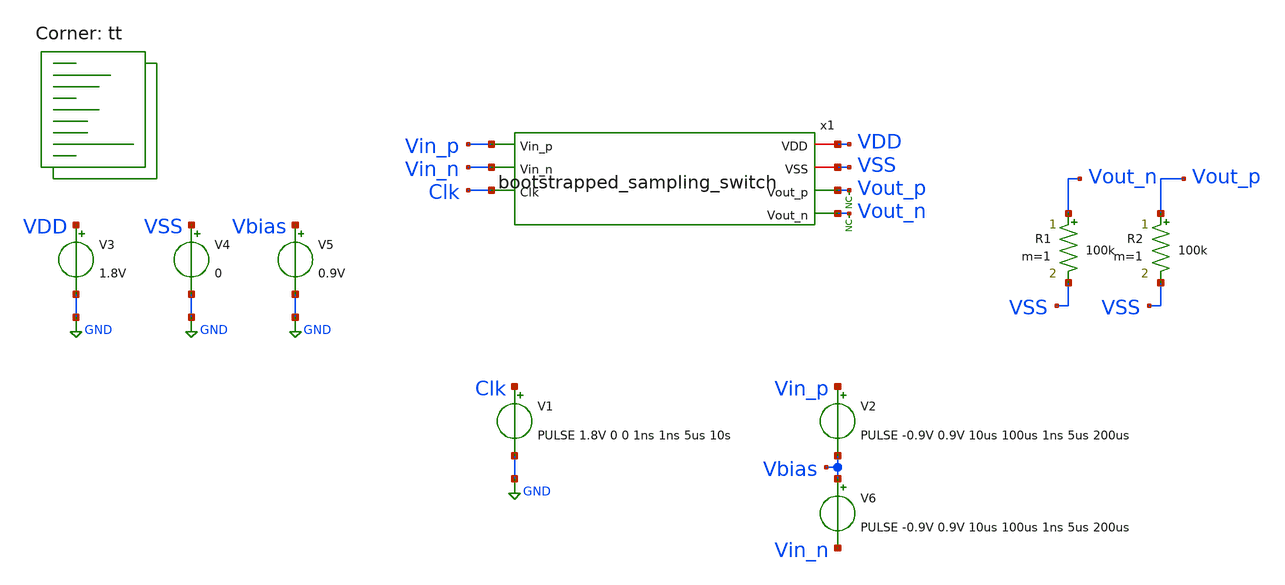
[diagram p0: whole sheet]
** sch_path: xschem/tests/bootstrapped_sampling_switch/bootstrapped_sampling_switch_load_test.sch
**.subckt bootstrapped_sampling_switch_load_test
V3 VDD GND 1.8V
V4 VSS GND 0
x1 VDD Vin_p VSS Vin_n Clk Vout_p Vout_n bootstrapped_sampling_switch
V1 Clk GND PULSE 1.8V 0 0 1ns 1ns 5us 10s
V2 Vin_p Vbias PULSE -0.9V 0.9V 10us 100us 1ns 5us 200us
* noconn Vout_p
* noconn Vout_n
V5 Vbias GND 0.9V
V6 Vbias Vin_n PULSE -0.9V 0.9V 10us 100us 1ns 5us 200us
R1 Vout_n VSS 100k m=1
R2 Vout_p VSS 100k m=1
**** begin user architecture code
 *.lib $::SKYWATER_MODELS/sky130.lib.spice tt
.include $::SKYWATER_STDCELLS/sky130_fd_sc_hd.spice


.options acct list
.temp 25
*vvcc VDD 0 dc 1.8
*vvss VSS 0 0
.control
save all
tran 0.1u 110u
*plot RST_PLS clk+2 Pulse+4
plot Vin_p-Vin_n Vout_p-Vout_n clk-4
plot Vout_p-Vout_n clk-4
plot Vout_p Vout_n clk-4
plot x1.net4-x1.net3
plot x1.net9-x1.net8
write bootstrapped_sampling_switch_load_test.raw
.endc


.lib $::SKYWATER_MODELS/sky130.lib.spice tt
**** end user architecture code
**.ends

* expanding   symbol:  src/bootstrapped_sampling_switch/bootstrapped_sampling_switch.sym # of pins=7
** sym_path: xschem/src/bootstrapped_sampling_switch/bootstrapped_sampling_switch.sym
** sch_path: xschem/src/bootstrapped_sampling_switch/bootstrapped_sampling_switch.sch
.subckt bootstrapped_sampling_switch VDD Vin_p VSS Vin_n Clk Vout_p Vout_n
*.iopin VDD
*.ipin Vin_p
*.opin Vout_p
*.iopin VSS
*.opin Vout_n
*.ipin Vin_n
*.ipin Clk
XM1 net3 Clk_n VSS VSS sky130_fd_pr__nfet_01v8 L=0.15 W=0.91 nf=1 ad='int((nf+1)/2) * W/nf * 0.29' as='int((nf+2)/2) * W/nf * 0.29'
+ pd='2*int((nf+1)/2) * (W/nf + 0.29)' ps='2*int((nf+2)/2) * (W/nf + 0.29)' nrd='0.29 / W' nrs='0.29 / W'
+ sa=0 sb=0 sd=0 mult=8 m=8
XM2 net1 Clk VDD VDD sky130_fd_pr__pfet_01v8 L=0.15 W=1.605 nf=1 ad='int((nf+1)/2) * W/nf * 0.29' as='int((nf+2)/2) * W/nf * 0.29'
+ pd='2*int((nf+1)/2) * (W/nf + 0.29)' ps='2*int((nf+2)/2) * (W/nf + 0.29)' nrd='0.29 / W' nrs='0.29 / W'
+ sa=0 sb=0 sd=0 mult=1 m=1
XM3 net1 Clk net3 VSS sky130_fd_pr__nfet_01v8 L=0.15 W=0.91 nf=1 ad='int((nf+1)/2) * W/nf * 0.29' as='int((nf+2)/2) * W/nf * 0.29'
+ pd='2*int((nf+1)/2) * (W/nf + 0.29)' ps='2*int((nf+2)/2) * (W/nf + 0.29)' nrd='0.29 / W' nrs='0.29 / W'
+ sa=0 sb=0 sd=0 mult=1 m=1
XC1 net2 net3 sky130_fd_pr__cap_mim_m3_1 W=30 L=30 MF=1 m=1
XM4 net2 net4 VDD net2 sky130_fd_pr__pfet_01v8 L=0.15 W=5 nf=1 ad='int((nf+1)/2) * W/nf * 0.29' as='int((nf+2)/2) * W/nf * 0.29'
+ pd='2*int((nf+1)/2) * (W/nf + 0.29)' ps='2*int((nf+2)/2) * (W/nf + 0.29)' nrd='0.29 / W' nrs='0.29 / W'
+ sa=0 sb=0 sd=0 mult=1 m=1
XM5 net4 net1 net2 net2 sky130_fd_pr__pfet_01v8 L=0.15 W=1.605 nf=1 ad='int((nf+1)/2) * W/nf * 0.29'
+ as='int((nf+2)/2) * W/nf * 0.29' pd='2*int((nf+1)/2) * (W/nf + 0.29)' ps='2*int((nf+2)/2) * (W/nf + 0.29)'
+ nrd='0.29 / W' nrs='0.29 / W' sa=0 sb=0 sd=0 mult=1 m=1
XM6 net1 net4 net3 VSS sky130_fd_pr__nfet_01v8 L=0.15 W=0.91 nf=1 ad='int((nf+1)/2) * W/nf * 0.29' as='int((nf+2)/2) * W/nf * 0.29'
+ pd='2*int((nf+1)/2) * (W/nf + 0.29)' ps='2*int((nf+2)/2) * (W/nf + 0.29)' nrd='0.29 / W' nrs='0.29 / W'
+ sa=0 sb=0 sd=0 mult=1 m=1
XM7 Vin_p net4 net3 VSS sky130_fd_pr__nfet_01v8 L=0.15 W=0.91 nf=1 ad='int((nf+1)/2) * W/nf * 0.29' as='int((nf+2)/2) * W/nf * 0.29'
+ pd='2*int((nf+1)/2) * (W/nf + 0.29)' ps='2*int((nf+2)/2) * (W/nf + 0.29)' nrd='0.29 / W' nrs='0.29 / W'
+ sa=0 sb=0 sd=0 mult=1 m=1
XM8 Vin_p net4 Vout_p VSS sky130_fd_pr__nfet_01v8 L=0.15 W=0.91 nf=1 ad='int((nf+1)/2) * W/nf * 0.29'
+ as='int((nf+2)/2) * W/nf * 0.29' pd='2*int((nf+1)/2) * (W/nf + 0.29)' ps='2*int((nf+2)/2) * (W/nf + 0.29)'
+ nrd='0.29 / W' nrs='0.29 / W' sa=0 sb=0 sd=0 mult=75 m=75
XM9 net4 VDD net5 VSS sky130_fd_pr__nfet_01v8 L=0.15 W=0.91 nf=1 ad='int((nf+1)/2) * W/nf * 0.29' as='int((nf+2)/2) * W/nf * 0.29'
+ pd='2*int((nf+1)/2) * (W/nf + 0.29)' ps='2*int((nf+2)/2) * (W/nf + 0.29)' nrd='0.29 / W' nrs='0.29 / W'
+ sa=0 sb=0 sd=0 mult=2 m=2
XM10 net5 Clk_n VSS VSS sky130_fd_pr__nfet_01v8 L=0.15 W=0.91 nf=1 ad='int((nf+1)/2) * W/nf * 0.29' as='int((nf+2)/2) * W/nf * 0.29'
+ pd='2*int((nf+1)/2) * (W/nf + 0.29)' ps='2*int((nf+2)/2) * (W/nf + 0.29)' nrd='0.29 / W' nrs='0.29 / W'
+ sa=0 sb=0 sd=0 mult=1 m=1
x1 Clk VSS VSS VDD VDD Clk_n sky130_fd_sc_hd__clkinv_1
XM11 net8 Clk_n VSS VSS sky130_fd_pr__nfet_01v8 L=0.15 W=0.91 nf=1 ad='int((nf+1)/2) * W/nf * 0.29' as='int((nf+2)/2) * W/nf * 0.29'
+ pd='2*int((nf+1)/2) * (W/nf + 0.29)' ps='2*int((nf+2)/2) * (W/nf + 0.29)' nrd='0.29 / W' nrs='0.29 / W'
+ sa=0 sb=0 sd=0 mult=8 m=8
XM12 net6 Clk VDD VDD sky130_fd_pr__pfet_01v8 L=0.15 W=1.605 nf=1 ad='int((nf+1)/2) * W/nf * 0.29' as='int((nf+2)/2) * W/nf * 0.29'
+ pd='2*int((nf+1)/2) * (W/nf + 0.29)' ps='2*int((nf+2)/2) * (W/nf + 0.29)' nrd='0.29 / W' nrs='0.29 / W'
+ sa=0 sb=0 sd=0 mult=1 m=1
XM13 net6 Clk net8 VSS sky130_fd_pr__nfet_01v8 L=0.15 W=0.91 nf=1 ad='int((nf+1)/2) * W/nf * 0.29' as='int((nf+2)/2) * W/nf * 0.29'
+ pd='2*int((nf+1)/2) * (W/nf + 0.29)' ps='2*int((nf+2)/2) * (W/nf + 0.29)' nrd='0.29 / W' nrs='0.29 / W'
+ sa=0 sb=0 sd=0 mult=1 m=1
XC2 net7 net8 sky130_fd_pr__cap_mim_m3_1 W=30 L=30 MF=1 m=1
XM14 net7 net9 VDD net7 sky130_fd_pr__pfet_01v8 L=0.15 W=5 nf=1 ad='int((nf+1)/2) * W/nf * 0.29' as='int((nf+2)/2) * W/nf * 0.29'
+ pd='2*int((nf+1)/2) * (W/nf + 0.29)' ps='2*int((nf+2)/2) * (W/nf + 0.29)' nrd='0.29 / W' nrs='0.29 / W'
+ sa=0 sb=0 sd=0 mult=1 m=1
XM15 net9 net6 net7 net7 sky130_fd_pr__pfet_01v8 L=0.15 W=1.605 nf=1 ad='int((nf+1)/2) * W/nf * 0.29'
+ as='int((nf+2)/2) * W/nf * 0.29' pd='2*int((nf+1)/2) * (W/nf + 0.29)' ps='2*int((nf+2)/2) * (W/nf + 0.29)'
+ nrd='0.29 / W' nrs='0.29 / W' sa=0 sb=0 sd=0 mult=1 m=1
XM16 net6 net9 net8 VSS sky130_fd_pr__nfet_01v8 L=0.15 W=0.91 nf=1 ad='int((nf+1)/2) * W/nf * 0.29' as='int((nf+2)/2) * W/nf * 0.29'
+ pd='2*int((nf+1)/2) * (W/nf + 0.29)' ps='2*int((nf+2)/2) * (W/nf + 0.29)' nrd='0.29 / W' nrs='0.29 / W'
+ sa=0 sb=0 sd=0 mult=1 m=1
XM17 Vin_n net9 net8 VSS sky130_fd_pr__nfet_01v8 L=0.15 W=0.91 nf=1 ad='int((nf+1)/2) * W/nf * 0.29'
+ as='int((nf+2)/2) * W/nf * 0.29' pd='2*int((nf+1)/2) * (W/nf + 0.29)' ps='2*int((nf+2)/2) * (W/nf + 0.29)'
+ nrd='0.29 / W' nrs='0.29 / W' sa=0 sb=0 sd=0 mult=1 m=1
XM18 Vin_n net9 Vout_n VSS sky130_fd_pr__nfet_01v8 L=0.15 W=0.91 nf=1 ad='int((nf+1)/2) * W/nf * 0.29'
+ as='int((nf+2)/2) * W/nf * 0.29' pd='2*int((nf+1)/2) * (W/nf + 0.29)' ps='2*int((nf+2)/2) * (W/nf + 0.29)'
+ nrd='0.29 / W' nrs='0.29 / W' sa=0 sb=0 sd=0 mult=75 m=75
XM19 net9 VDD net10 VSS sky130_fd_pr__nfet_01v8 L=0.15 W=0.91 nf=1 ad='int((nf+1)/2) * W/nf * 0.29' as='int((nf+2)/2) * W/nf * 0.29'
+ pd='2*int((nf+1)/2) * (W/nf + 0.29)' ps='2*int((nf+2)/2) * (W/nf + 0.29)' nrd='0.29 / W' nrs='0.29 / W'
+ sa=0 sb=0 sd=0 mult=2 m=2
XM20 net10 Clk_n VSS VSS sky130_fd_pr__nfet_01v8 L=0.15 W=0.91 nf=1 ad='int((nf+1)/2) * W/nf * 0.29'
+ as='int((nf+2)/2) * W/nf * 0.29' pd='2*int((nf+1)/2) * (W/nf + 0.29)' ps='2*int((nf+2)/2) * (W/nf + 0.29)'
+ nrd='0.29 / W' nrs='0.29 / W' sa=0 sb=0 sd=0 mult=1 m=1
.ends

.GLOBAL GND
.end
